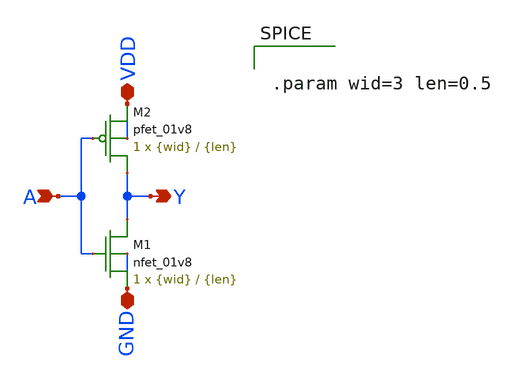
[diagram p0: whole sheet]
** sch_path: final/schematics/inverter.sch
**.subckt inverter A VDD GND Y
*.ipin A
*.iopin VDD
*.iopin GND
*.opin Y
XM1 Y A GND GND sky130_fd_pr__nfet_01v8 L={len} W={wid} nf=1 ad='int((nf+1)/2) * W/nf * 0.29' as='int((nf+2)/2) * W/nf * 0.29'
+ pd='2*int((nf+1)/2) * (W/nf + 0.29)' ps='2*int((nf+2)/2) * (W/nf + 0.29)' nrd='0.29 / W' nrs='0.29 / W'
+ sa=0 sb=0 sd=0 mult=1 m=1
XM2 Y A VDD VDD sky130_fd_pr__pfet_01v8 L={len} W={wid} nf=1 ad='int((nf+1)/2) * W/nf * 0.29' as='int((nf+2)/2) * W/nf * 0.29'
+ pd='2*int((nf+1)/2) * (W/nf + 0.29)' ps='2*int((nf+2)/2) * (W/nf + 0.29)' nrd='0.29 / W' nrs='0.29 / W'
+ sa=0 sb=0 sd=0 mult=1 m=1
**** begin user architecture code


.param wid=3 len=0.5


**** end user architecture code
**.ends
.end
